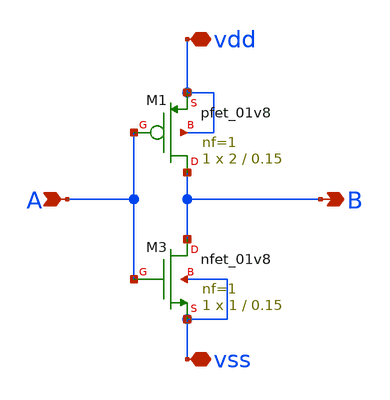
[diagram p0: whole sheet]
** sch_path: xschem/src/inverter/inverter.sch
**.subckt inverter vdd vss A B
*.iopin vdd
*.iopin vss
*.ipin A
*.opin B
XM3 B A vss vss sky130_fd_pr__nfet_01v8 L=0.15 W=1 nf=1 ad='int((nf+1)/2) * W/nf * 0.29' as='int((nf+2)/2) * W/nf * 0.29'
+ pd='2*int((nf+1)/2) * (W/nf + 0.29)' ps='2*int((nf+2)/2) * (W/nf + 0.29)' nrd='0.29 / W' nrs='0.29 / W'
+ sa=0 sb=0 sd=0 mult=1 m=1
XM1 B A vdd vdd sky130_fd_pr__pfet_01v8 L=0.15 W=2 nf=1 ad='int((nf+1)/2) * W/nf * 0.29' as='int((nf+2)/2) * W/nf * 0.29'
+ pd='2*int((nf+1)/2) * (W/nf + 0.29)' ps='2*int((nf+2)/2) * (W/nf + 0.29)' nrd='0.29 / W' nrs='0.29 / W'
+ sa=0 sb=0 sd=0 mult=1 m=1
**.ends
.end
